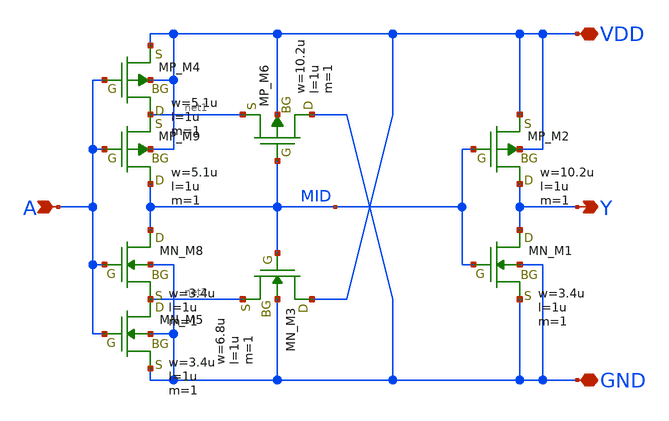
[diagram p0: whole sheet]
** sch_path: LEF/BUFTH.sch
**.subckt BUFTH A Y VDD GND
*.ipin A
*.opin Y
*.iopin VDD
*.iopin GND
XM9 MID A net1 VDD PMOS w=5.1u l=1u as=0 ad=0 ps=0 pd=0 nrd=0 nrs=0 m=1
XM2 Y MID VDD VDD PMOS w=10.2u l=1u as=0 ad=0 ps=0 pd=0 nrd=0 nrs=0 m=1
XM8 MID A net2 GND NMOS w=3.4u l=1u as=0 ad=0 ps=0 pd=0 nrd=0 nrs=0 m=1
XM1 Y MID GND GND NMOS w=3.4u l=1u as=0 ad=0 ps=0 pd=0 nrd=0 nrs=0 m=1
XM6 GND MID net1 VDD PMOS w=10.2u l=1u as=0 ad=0 ps=0 pd=0 nrd=0 nrs=0 m=1
XM3 VDD MID net2 GND NMOS w=6.8u l=1u as=0 ad=0 ps=0 pd=0 nrd=0 nrs=0 m=1
XM5 net2 A GND GND NMOS w=3.4u l=1u as=0 ad=0 ps=0 pd=0 nrd=0 nrs=0 m=1
XM4 net1 A VDD VDD PMOS w=5.1u l=1u as=0 ad=0 ps=0 pd=0 nrd=0 nrs=0 m=1
**.ends
.end
